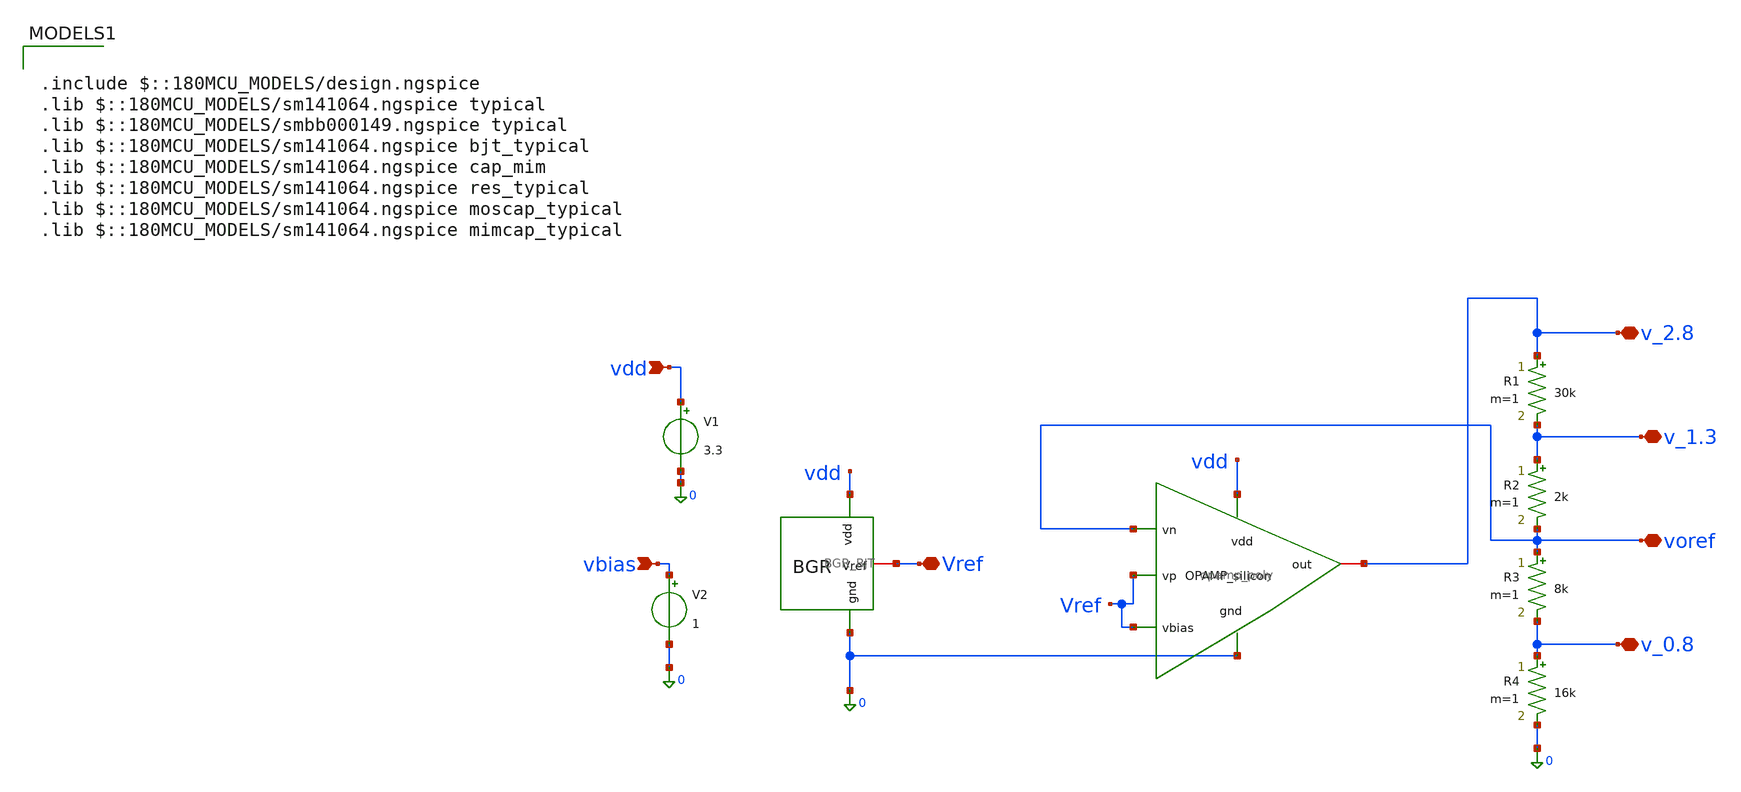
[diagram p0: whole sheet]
** sch_path: xschem/bias_generator/BGR_OP.sch
**.subckt BGR_OP vdd Vref v_1.3 voref v_0.8 v_2.8 vbias
*.ipin vdd
*.iopin Vref
*.iopin v_1.3
*.iopin voref
*.iopin v_0.8
*.iopin v_2.8
*.ipin vbias
V1 vdd 0 3.3
x2 vdd voref 0 v_2.8 Vref Vref opamp_poly
R1 v_2.8 v_1.3 30k m=1
R2 v_1.3 voref 2k m=1
R3 voref v_0.8 8k m=1
R4 v_0.8 0 16k m=1
x1 vdd Vref 0 BGR_BJT
V2 vbias 0 1
**** begin user architecture code


.param  w1=80u       l1=6u  w2=26u       l2=1u  w3=78u     l3=0.7u  w4=60u       l4=4u  w5=60u
+      l5=4u  w6=26u       l6=1u  w7=72u    l7=0.3u
.control
save all
op
write BGR_OP.raw
set appendwrite
tran 1n 30u
set color0=white
set color1=black
plot v(v_2.8) v(v_1.3) v(voref) v(v_0.8)
write BGR_OP.raw
.endc



.include $::180MCU_MODELS/design.ngspice
.lib $::180MCU_MODELS/sm141064.ngspice typical
.lib $::180MCU_MODELS/smbb000149.ngspice typical
.lib $::180MCU_MODELS/sm141064.ngspice bjt_typical
.lib $::180MCU_MODELS/sm141064.ngspice cap_mim
.lib $::180MCU_MODELS/sm141064.ngspice res_typical
.lib $::180MCU_MODELS/sm141064.ngspice moscap_typical
.lib $::180MCU_MODELS/sm141064.ngspice mimcap_typical

**** end user architecture code
**.ends

* expanding   symbol:  GF180/xschem/Chipathon/OpAMP_Silicon/opamp_poly.sym # of pins=6
** sym_path: OpAmP/opamp_poly.sym
** sch_path: OpAmP/opamp_poly.sch
.subckt opamp_poly vdd vn gnd out vp vbias
*.ipin gnd
*.iopin out
*.ipin vbias
*.ipin vp
*.ipin vn
*.ipin vdd
XM1 net3 vbias gnd gnd nfet_03v3 L=l1 W=w1 nf=1 ad='int((nf+1)/2) * W/nf * 0.18u' as='int((nf+2)/2) * W/nf * 0.18u'
+ pd='2*int((nf+1)/2) * (W/nf + 0.18u)' ps='2*int((nf+2)/2) * (W/nf + 0.18u)' nrd='0.18u / W' nrs='0.18u / W'
+ sa=0 sb=0 sd=0 m=1
XM2 net2 net2 vdd vdd pfet_03v3 L=l2 W=w2 nf=1 ad='int((nf+1)/2) * W/nf * 0.18u' as='int((nf+2)/2) * W/nf * 0.18u'
+ pd='2*int((nf+1)/2) * (W/nf + 0.18u)' ps='2*int((nf+2)/2) * (W/nf + 0.18u)' nrd='0.18u / W' nrs='0.18u / W'
+ sa=0 sb=0 sd=0 m=1
XM3 out vbias gnd gnd nfet_03v3 L=l3 W=w3 nf=1 ad='int((nf+1)/2) * W/nf * 0.18u' as='int((nf+2)/2) * W/nf * 0.18u'
+ pd='2*int((nf+1)/2) * (W/nf + 0.18u)' ps='2*int((nf+2)/2) * (W/nf + 0.18u)' nrd='0.18u / W' nrs='0.18u / W'
+ sa=0 sb=0 sd=0 m=1
XM4 net2 vn net3 gnd nfet_03v3 L=l4 W=w4 nf=1 ad='int((nf+1)/2) * W/nf * 0.18u' as='int((nf+2)/2) * W/nf * 0.18u'
+ pd='2*int((nf+1)/2) * (W/nf + 0.18u)' ps='2*int((nf+2)/2) * (W/nf + 0.18u)' nrd='0.18u / W' nrs='0.18u / W'
+ sa=0 sb=0 sd=0 m=1
XM5 net1 vp net3 gnd nfet_03v3 L=l5 W=w5 nf=1 ad='int((nf+1)/2) * W/nf * 0.18u' as='int((nf+2)/2) * W/nf * 0.18u'
+ pd='2*int((nf+1)/2) * (W/nf + 0.18u)' ps='2*int((nf+2)/2) * (W/nf + 0.18u)' nrd='0.18u / W' nrs='0.18u / W'
+ sa=0 sb=0 sd=0 m=1
XM6 net1 net2 vdd vdd pfet_03v3 L=l6 W=w6 nf=1 ad='int((nf+1)/2) * W/nf * 0.18u' as='int((nf+2)/2) * W/nf * 0.18u'
+ pd='2*int((nf+1)/2) * (W/nf + 0.18u)' ps='2*int((nf+2)/2) * (W/nf + 0.18u)' nrd='0.18u / W' nrs='0.18u / W'
+ sa=0 sb=0 sd=0 m=1
XM7 out net1 vdd vdd pfet_03v3 L=l7 W=w7 nf=1 ad='int((nf+1)/2) * W/nf * 0.18u' as='int((nf+2)/2) * W/nf * 0.18u'
+ pd='2*int((nf+1)/2) * (W/nf + 0.18u)' ps='2*int((nf+2)/2) * (W/nf + 0.18u)' nrd='0.18u / W' nrs='0.18u / W'
+ sa=0 sb=0 sd=0 m=1
XR1 net4 net1 gnd ppolyf_u_1k r_width=3e-6 r_length=6.6e-6 m=1
XC1 out net4 cap_mim_1f5fF c_width=20e-6 c_length=20e-6 m=1
.ends


* expanding   symbol:  GF180/xschem/Chipathon/BGR/BGR_BJT.sym # of pins=3
** sym_path: xschem/bias_generator/BGR_BJT.sym
** sch_path: xschem/bias_generator/BGR_BJT.sch
.subckt BGR_BJT vdd Vref gnd
*.ipin gnd
*.iopin Vref
*.ipin vdd
XM2 net1 net2 vdd vdd pfet_03v3 L=4u W=10u nf=1 ad='int((nf+1)/2) * W/nf * 0.18u' as='int((nf+2)/2) * W/nf * 0.18u'
+ pd='2*int((nf+1)/2) * (W/nf + 0.18u)' ps='2*int((nf+2)/2) * (W/nf + 0.18u)' nrd='0.18u / W' nrs='0.18u / W'
+ sa=0 sb=0 sd=0 m=1
XM3 net2 net2 vdd vdd pfet_03v3 L=4u W=10u nf=1 ad='int((nf+1)/2) * W/nf * 0.18u' as='int((nf+2)/2) * W/nf * 0.18u'
+ pd='2*int((nf+1)/2) * (W/nf + 0.18u)' ps='2*int((nf+2)/2) * (W/nf + 0.18u)' nrd='0.18u / W' nrs='0.18u / W'
+ sa=0 sb=0 sd=0 m=1
XM4 Vref net2 vdd vdd pfet_03v3 L=4u W=10u nf=1 ad='int((nf+1)/2) * W/nf * 0.18u' as='int((nf+2)/2) * W/nf * 0.18u'
+ pd='2*int((nf+1)/2) * (W/nf + 0.18u)' ps='2*int((nf+2)/2) * (W/nf + 0.18u)' nrd='0.18u / W' nrs='0.18u / W'
+ sa=0 sb=0 sd=0 m=1
XM13 net1 net1 net5 gnd nfet_03v3 L=2u W=10u nf=1 ad='int((nf+1)/2) * W/nf * 0.18u' as='int((nf+2)/2) * W/nf * 0.18u'
+ pd='2*int((nf+1)/2) * (W/nf + 0.18u)' ps='2*int((nf+2)/2) * (W/nf + 0.18u)' nrd='0.18u / W' nrs='0.18u / W'
+ sa=0 sb=0 sd=0 m=1
XM14 net2 net1 net4 gnd nfet_03v3 L=2u W=10u nf=1 ad='int((nf+1)/2) * W/nf * 0.18u' as='int((nf+2)/2) * W/nf * 0.18u'
+ pd='2*int((nf+1)/2) * (W/nf + 0.18u)' ps='2*int((nf+2)/2) * (W/nf + 0.18u)' nrd='0.18u / W' nrs='0.18u / W'
+ sa=0 sb=0 sd=0 m=1
R1 Vref net7 66k m=1
R2 net4 net3 5k m=1
XQ1 gnd gnd net3 pnp_05p00x05p00 m=4 par=4
XQ2 gnd gnd net5 pnp_05p00x05p00 m=1 par=1
XM1 net2 net6 gnd gnd nfet_03v3 L=2u W=10u nf=1 ad='int((nf+1)/2) * W/nf * 0.18u' as='int((nf+2)/2) * W/nf * 0.18u'
+ pd='2*int((nf+1)/2) * (W/nf + 0.18u)' ps='2*int((nf+2)/2) * (W/nf + 0.18u)' nrd='0.18u / W' nrs='0.18u / W'
+ sa=0 sb=0 sd=0 m=1
XM5 vdd vdd net6 gnd nfet_03v3 L=0.5u W=1u nf=1 ad='int((nf+1)/2) * W/nf * 0.18u' as='int((nf+2)/2) * W/nf * 0.18u'
+ pd='2*int((nf+1)/2) * (W/nf + 0.18u)' ps='2*int((nf+2)/2) * (W/nf + 0.18u)' nrd='0.18u / W' nrs='0.18u / W'
+ sa=0 sb=0 sd=0 m=1
XM6 net6 net1 gnd gnd nfet_03v3 L=1u W=20u nf=1 ad='int((nf+1)/2) * W/nf * 0.18u' as='int((nf+2)/2) * W/nf * 0.18u'
+ pd='2*int((nf+1)/2) * (W/nf + 0.18u)' ps='2*int((nf+2)/2) * (W/nf + 0.18u)' nrd='0.18u / W' nrs='0.18u / W'
+ sa=0 sb=0 sd=0 m=1
XQ3 gnd gnd net7 pnp_05p00x05p00 m=1 par=1
.ends

.end
